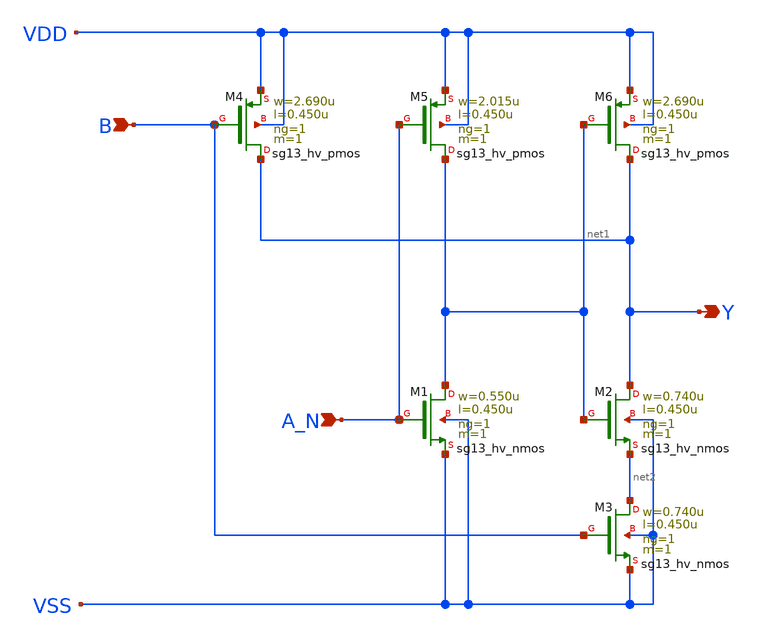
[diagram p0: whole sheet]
** sch_path: ihp-sg13g2/libs.ref/sg13g2_stdcell_hv/sch/xschem/sg13g2_hv_nand2b_1.sch
* Copyright 2023 IHP PDK Authors
* Licensed under the Apache License, Version 2.0 (the "License");
* you may not use this file except in compliance with the License.
* You may obtain a copy of the License at
* https://www.apache.org/licenses/LICENSE-2.0
* Unless required by applicable law or agreed to in writing, software
* distributed under the License is distributed on an "AS IS" BASIS,
* WITHOUT WARRANTIES OR CONDITIONS OF ANY KIND, either express or implied.
* See the License for the specific language governing permissions and
* limitations under the License.
**.subckt sg13g2_hv_nand2b_1 Y B A_N
*.opin Y
*.ipin B
*.ipin A_N
XM1 net1 A_N VSS VSS sg13_hv_nmos w=0.550u l=0.450u ng=1 m=1 mm_ok=1
XM2 Y net1 net2 VSS sg13_hv_nmos w=0.740u l=0.450u ng=1 m=1 mm_ok=1
XM3 net2 B VSS VSS sg13_hv_nmos w=0.740u l=0.450u ng=1 m=1 mm_ok=1
XM4 Y B VDD VDD sg13_hv_pmos w=2.690u l=0.450u ng=1 m=1 mm_ok=1
XM5 net1 A_N VDD VDD sg13_hv_pmos w=2.015u l=0.450u ng=1 m=1 mm_ok=1
XM6 Y net1 VDD VDD sg13_hv_pmos w=2.690u l=0.450u ng=1 m=1 mm_ok=1
**.ends
.end
